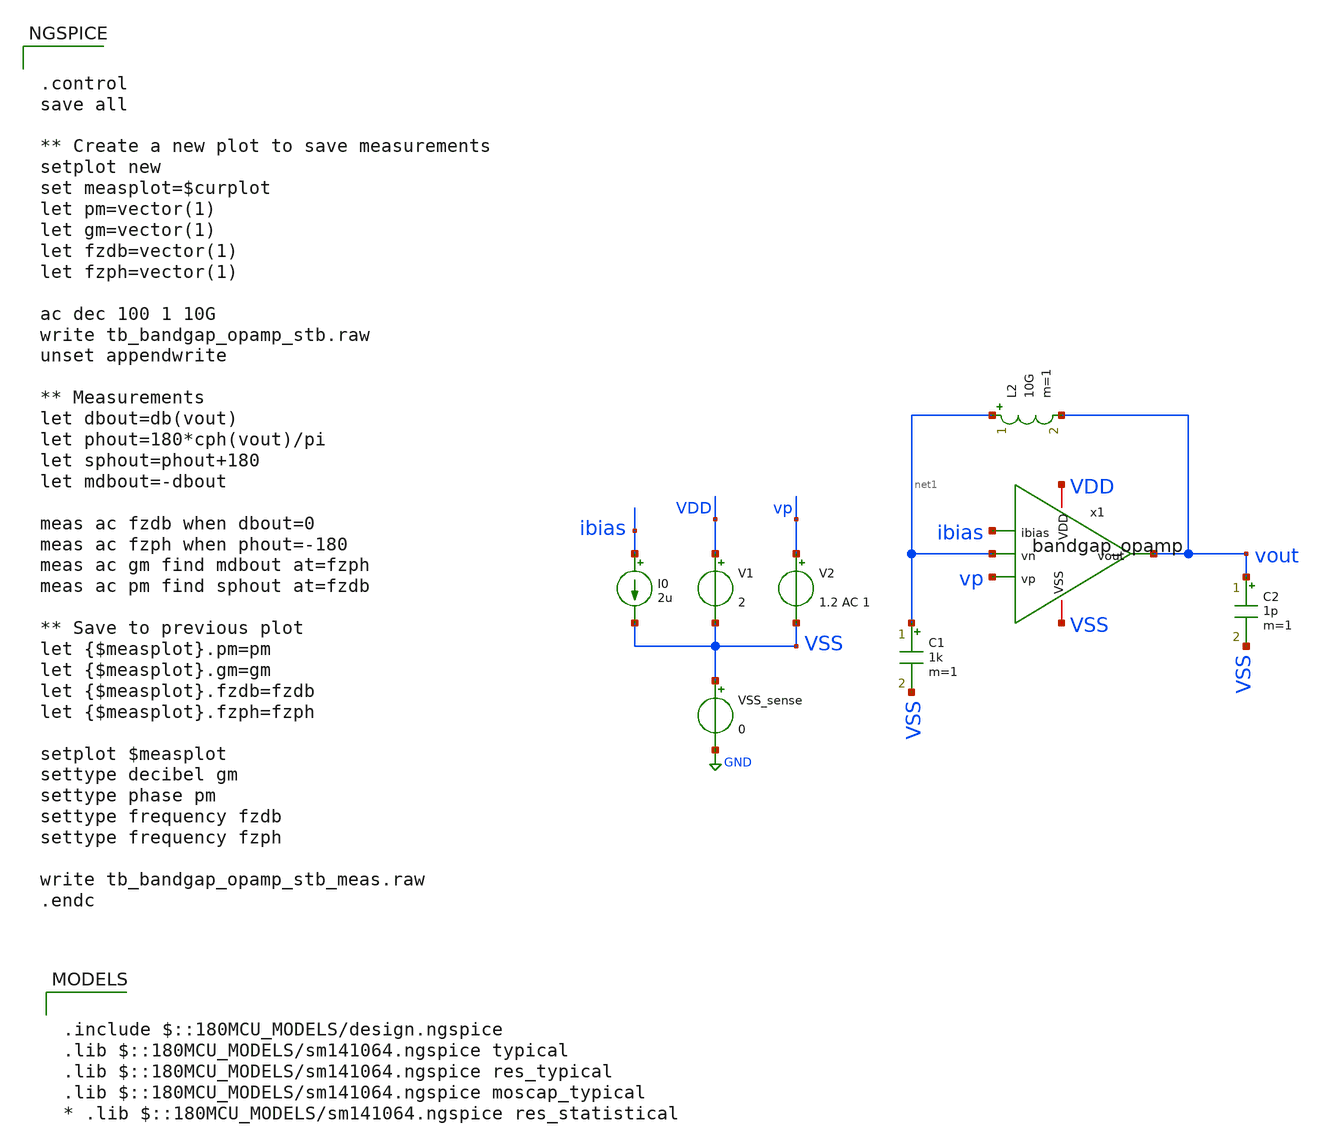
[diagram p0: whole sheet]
** sch_path: designs/libs/tb_bandgap/tb_bandgap_opamp_stb/tb_bandgap_opamp_stb.sch
**.subckt tb_bandgap_opamp_stb
C1 net1 VSS 1k m=1
V1 VDD VSS 2
V2 vp VSS 1.2 AC 1
VSS_sense VSS GND 0
C2 vout VSS 1p m=1
L2 net1 vout 10G m=1
I0 ibias VSS 2u
x1 VDD ibias net1 vp vout VSS bandgap_opamp
**** begin user architecture code

.include $::180MCU_MODELS/design.ngspice
.lib $::180MCU_MODELS/sm141064.ngspice typical
.lib $::180MCU_MODELS/sm141064.ngspice res_typical
.lib $::180MCU_MODELS/sm141064.ngspice moscap_typical
* .lib $::180MCU_MODELS/sm141064.ngspice res_statistical



.control
save all

** Create a new plot to save measurements
setplot new
set measplot=$curplot
let pm=vector(1)
let gm=vector(1)
let fzdb=vector(1)
let fzph=vector(1)

ac dec 100 1 10G
write tb_bandgap_opamp_stb.raw
unset appendwrite

** Measurements
let dbout=db(vout)
let phout=180*cph(vout)/pi
let sphout=phout+180
let mdbout=-dbout

meas ac fzdb when dbout=0
meas ac fzph when phout=-180
meas ac gm find mdbout at=fzph
meas ac pm find sphout at=fzdb

** Save to previous plot
let {$measplot}.pm=pm
let {$measplot}.gm=gm
let {$measplot}.fzdb=fzdb
let {$measplot}.fzph=fzph

setplot $measplot
settype decibel gm
settype phase pm
settype frequency fzdb
settype frequency fzph

write tb_bandgap_opamp_stb_meas.raw
.endc


**** end user architecture code
**.ends

* expanding   symbol:  libs/core_bandgap/bandgap_opamp/bandgap_opamp.sym # of pins=6
** sym_path: designs/libs/core_bandgap/bandgap_opamp/bandgap_opamp.sym
** sch_path: designs/libs/core_bandgap/bandgap_opamp/bandgap_opamp.sch
.subckt bandgap_opamp VDD ibias vn vp vout VSS
*.ipin vn
*.ipin vp
*.opin vout
*.ipin ibias
*.iopin VDD
*.iopin VSS
XC1 vout net3 cap_nmos_03v3_b c_width=15u c_length=15u m=1
XM9 ibias ibias VDD VDD pfet_05v0 L=1u W=1u nf=1 ad='int((nf+1)/2) * W/nf * 0.18u' as='int((nf+2)/2) * W/nf * 0.18u'
+ pd='2*int((nf+1)/2) * (W/nf + 0.18u)' ps='2*int((nf+2)/2) * (W/nf + 0.18u)' nrd='0.18u / W' nrs='0.18u / W'
+ sa=0 sb=0 sd=0 m=1
XM10 net2 net2 VSS VSS nfet_05v0 L=2u W=1u nf=1 ad='int((nf+1)/2) * W/nf * 0.18u' as='int((nf+2)/2) * W/nf * 0.18u'
+ pd='2*int((nf+1)/2) * (W/nf + 0.18u)' ps='2*int((nf+2)/2) * (W/nf + 0.18u)' nrd='0.18u / W' nrs='0.18u / W'
+ sa=0 sb=0 sd=0 m=1
XM3 net1 ibias VDD VDD pfet_05v0 L=1u W=1u nf=1 ad='int((nf+1)/2) * W/nf * 0.18u' as='int((nf+2)/2) * W/nf * 0.18u'
+ pd='2*int((nf+1)/2) * (W/nf + 0.18u)' ps='2*int((nf+2)/2) * (W/nf + 0.18u)' nrd='0.18u / W' nrs='0.18u / W'
+ sa=0 sb=0 sd=0 m=1
XM4 vout ibias VDD VDD pfet_05v0 L=1u W=1u nf=1 ad='int((nf+1)/2) * W/nf * 0.18u' as='int((nf+2)/2) * W/nf * 0.18u'
+ pd='2*int((nf+1)/2) * (W/nf + 0.18u)' ps='2*int((nf+2)/2) * (W/nf + 0.18u)' nrd='0.18u / W' nrs='0.18u / W'
+ sa=0 sb=0 sd=0 m=4
XM1 net2 vn net1 VDD pfet_05v0 L=1u W=4u nf=1 ad='int((nf+1)/2) * W/nf * 0.18u' as='int((nf+2)/2) * W/nf * 0.18u'
+ pd='2*int((nf+1)/2) * (W/nf + 0.18u)' ps='2*int((nf+2)/2) * (W/nf + 0.18u)' nrd='0.18u / W' nrs='0.18u / W'
+ sa=0 sb=0 sd=0 m=1
XM2 net3 vp net1 VDD pfet_05v0 L=1u W=4u nf=1 ad='int((nf+1)/2) * W/nf * 0.18u' as='int((nf+2)/2) * W/nf * 0.18u'
+ pd='2*int((nf+1)/2) * (W/nf + 0.18u)' ps='2*int((nf+2)/2) * (W/nf + 0.18u)' nrd='0.18u / W' nrs='0.18u / W'
+ sa=0 sb=0 sd=0 m=1
XM5 net3 net2 VSS VSS nfet_05v0 L=2u W=1u nf=1 ad='int((nf+1)/2) * W/nf * 0.18u' as='int((nf+2)/2) * W/nf * 0.18u'
+ pd='2*int((nf+1)/2) * (W/nf + 0.18u)' ps='2*int((nf+2)/2) * (W/nf + 0.18u)' nrd='0.18u / W' nrs='0.18u / W'
+ sa=0 sb=0 sd=0 m=1
XM6 vout net3 VSS VSS nfet_05v0 L=2u W=1u nf=1 ad='int((nf+1)/2) * W/nf * 0.18u' as='int((nf+2)/2) * W/nf * 0.18u'
+ pd='2*int((nf+1)/2) * (W/nf + 0.18u)' ps='2*int((nf+2)/2) * (W/nf + 0.18u)' nrd='0.18u / W' nrs='0.18u / W'
+ sa=0 sb=0 sd=0 m=8
.ends

.GLOBAL GND
.end
